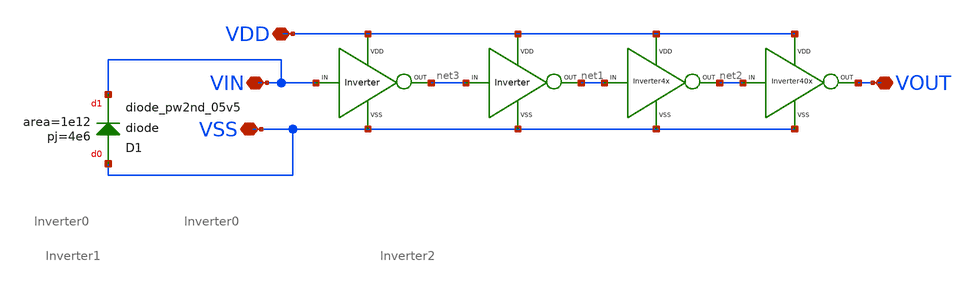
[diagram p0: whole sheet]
** sch_path: xschem/DC_DC_Converter_xschem/DC_DC_Converter/BUFFER/BUFFER_NMOS/BUFFER_N.sch
**.subckt BUFFER_N VDD VIN VSS VOUT
*.iopin VDD
*.iopin VIN
*.iopin VSS
*.iopin VOUT
X7 net3 net1 VDD VSS Inverter0
X8 net1 net2 VDD VSS Inverter1
X79 net2 VOUT VDD VSS Inverter2
X29 VIN net3 VDD VSS Inverter0
XD1 VSS VIN sky130_fd_pr__diode_pw2nd_05v5 area=1e12 pj=4e6
**.ends
.end
